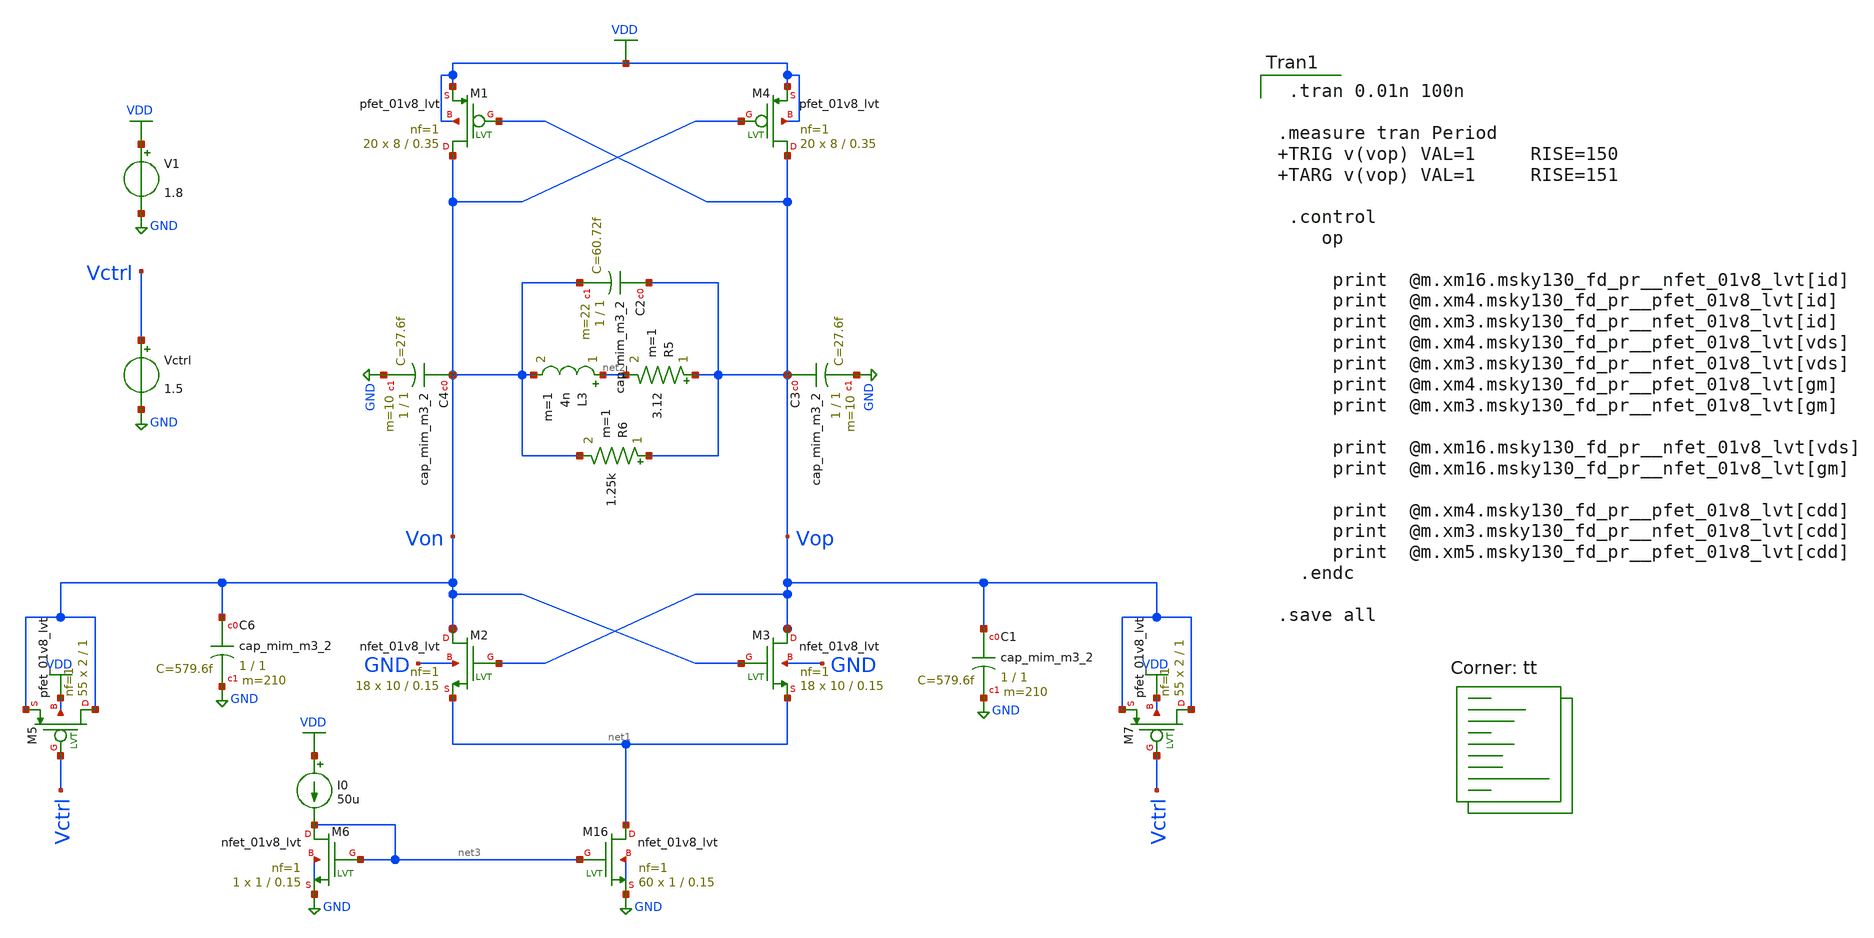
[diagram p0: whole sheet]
** sch_path: pll/lc_vco_lib_Hossam_Tarek/lc_osc_complementary_pmos/xschem/Complementary_0.5_1.5.sch
**.subckt Complementary_0.5_1.5
XM2 Von Vop net1 GND sky130_fd_pr__nfet_01v8_lvt L=0.15 W=10 nf=1 ad='int((nf+1)/2) * W/nf * 0.29' as='int((nf+2)/2) * W/nf * 0.29'
+ pd='2*int((nf+1)/2) * (W/nf + 0.29)' ps='2*int((nf+2)/2) * (W/nf + 0.29)' nrd='0.29 / W' nrs='0.29 / W'
+ sa=0 sb=0 sd=0 mult=18 m=18
XM3 Vop Von net1 GND sky130_fd_pr__nfet_01v8_lvt L=0.15 W=10 nf=1 ad='int((nf+1)/2) * W/nf * 0.29' as='int((nf+2)/2) * W/nf * 0.29'
+ pd='2*int((nf+1)/2) * (W/nf + 0.29)' ps='2*int((nf+2)/2) * (W/nf + 0.29)' nrd='0.29 / W' nrs='0.29 / W'
+ sa=0 sb=0 sd=0 mult=18 m=18
V1 VDD GND 1.8
L3 net2 Von 4n m=1
R5 Vop net2 3.12 m=1
R6 Vop Von 1.25k m=1
XC2 Vop Von sky130_fd_pr__cap_mim_m3_2 W=1 L=1 MF=22 m=22
XM7 Vop Vctrl Vop VDD sky130_fd_pr__pfet_01v8_lvt L=1 W=2 nf=1 ad='int((nf+1)/2) * W/nf * 0.29' as='int((nf+2)/2) * W/nf * 0.29'
+ pd='2*int((nf+1)/2) * (W/nf + 0.29)' ps='2*int((nf+2)/2) * (W/nf + 0.29)' nrd='0.29 / W' nrs='0.29 / W'
+ sa=0 sb=0 sd=0 mult=55 m=55
XM5 Von Vctrl Von VDD sky130_fd_pr__pfet_01v8_lvt L=1 W=2 nf=1 ad='int((nf+1)/2) * W/nf * 0.29' as='int((nf+2)/2) * W/nf * 0.29'
+ pd='2*int((nf+1)/2) * (W/nf + 0.29)' ps='2*int((nf+2)/2) * (W/nf + 0.29)' nrd='0.29 / W' nrs='0.29 / W'
+ sa=0 sb=0 sd=0 mult=55 m=55
Vctrl Vctrl GND 1.5
XM4 Vop Von VDD VDD sky130_fd_pr__pfet_01v8_lvt L=0.35 W=8 nf=1 ad='int((nf+1)/2) * W/nf * 0.29' as='int((nf+2)/2) * W/nf * 0.29'
+ pd='2*int((nf+1)/2) * (W/nf + 0.29)' ps='2*int((nf+2)/2) * (W/nf + 0.29)' nrd='0.29 / W' nrs='0.29 / W'
+ sa=0 sb=0 sd=0 mult=20 m=20
XM1 Von Vop VDD VDD sky130_fd_pr__pfet_01v8_lvt L=0.35 W=8 nf=1 ad='int((nf+1)/2) * W/nf * 0.29' as='int((nf+2)/2) * W/nf * 0.29'
+ pd='2*int((nf+1)/2) * (W/nf + 0.29)' ps='2*int((nf+2)/2) * (W/nf + 0.29)' nrd='0.29 / W' nrs='0.29 / W'
+ sa=0 sb=0 sd=0 mult=20 m=20
XM6 net3 net3 GND GND sky130_fd_pr__nfet_01v8_lvt L=0.15 W=1 nf=1 ad='int((nf+1)/2) * W/nf * 0.29' as='int((nf+2)/2) * W/nf * 0.29'
+ pd='2*int((nf+1)/2) * (W/nf + 0.29)' ps='2*int((nf+2)/2) * (W/nf + 0.29)' nrd='0.29 / W' nrs='0.29 / W'
+ sa=0 sb=0 sd=0 mult=1 m=1
XM16 net1 net3 GND GND sky130_fd_pr__nfet_01v8_lvt L=0.15 W=1 nf=1 ad='int((nf+1)/2) * W/nf * 0.29' as='int((nf+2)/2) * W/nf * 0.29'
+ pd='2*int((nf+1)/2) * (W/nf + 0.29)' ps='2*int((nf+2)/2) * (W/nf + 0.29)' nrd='0.29 / W' nrs='0.29 / W'
+ sa=0 sb=0 sd=0 mult=60 m=60
I0 VDD net3 50u
XC6 Von GND sky130_fd_pr__cap_mim_m3_2 W=1 L=1 MF=210 m=210
XC1 Vop GND sky130_fd_pr__cap_mim_m3_2 W=1 L=1 MF=210 m=210
XC3 Vop GND sky130_fd_pr__cap_mim_m3_2 W=1 L=1 MF=10 m=10
XC4 Von GND sky130_fd_pr__cap_mim_m3_2 W=1 L=1 MF=10 m=10
**** begin user architecture code
.lib $::SKYWATER_MODELS/sky130.lib.spice tt

 .tran 0.01n 100n

.measure tran Period  TRIG v(vop) VAL=1     RISE=150 TARG v(vop) VAL=1     RISE=151

 .control
    op

     print  @m.xm16.msky130_fd_pr__nfet_01v8_lvt[id]
     print  @m.xm4.msky130_fd_pr__pfet_01v8_lvt[id]
     print  @m.xm3.msky130_fd_pr__nfet_01v8_lvt[id]
     print  @m.xm4.msky130_fd_pr__pfet_01v8_lvt[vds]
     print  @m.xm3.msky130_fd_pr__nfet_01v8_lvt[vds]
     print  @m.xm4.msky130_fd_pr__pfet_01v8_lvt[gm]
     print  @m.xm3.msky130_fd_pr__nfet_01v8_lvt[gm]

     print  @m.xm16.msky130_fd_pr__nfet_01v8_lvt[vds]
     print  @m.xm16.msky130_fd_pr__nfet_01v8_lvt[gm]

     print  @m.xm4.msky130_fd_pr__pfet_01v8_lvt[cdd]
     print  @m.xm3.msky130_fd_pr__nfet_01v8_lvt[cdd]
     print  @m.xm5.msky130_fd_pr__pfet_01v8_lvt[cdd]
  .endc

.save all

**** end user architecture code
**.ends
.GLOBAL GND
.GLOBAL VDD
.end
